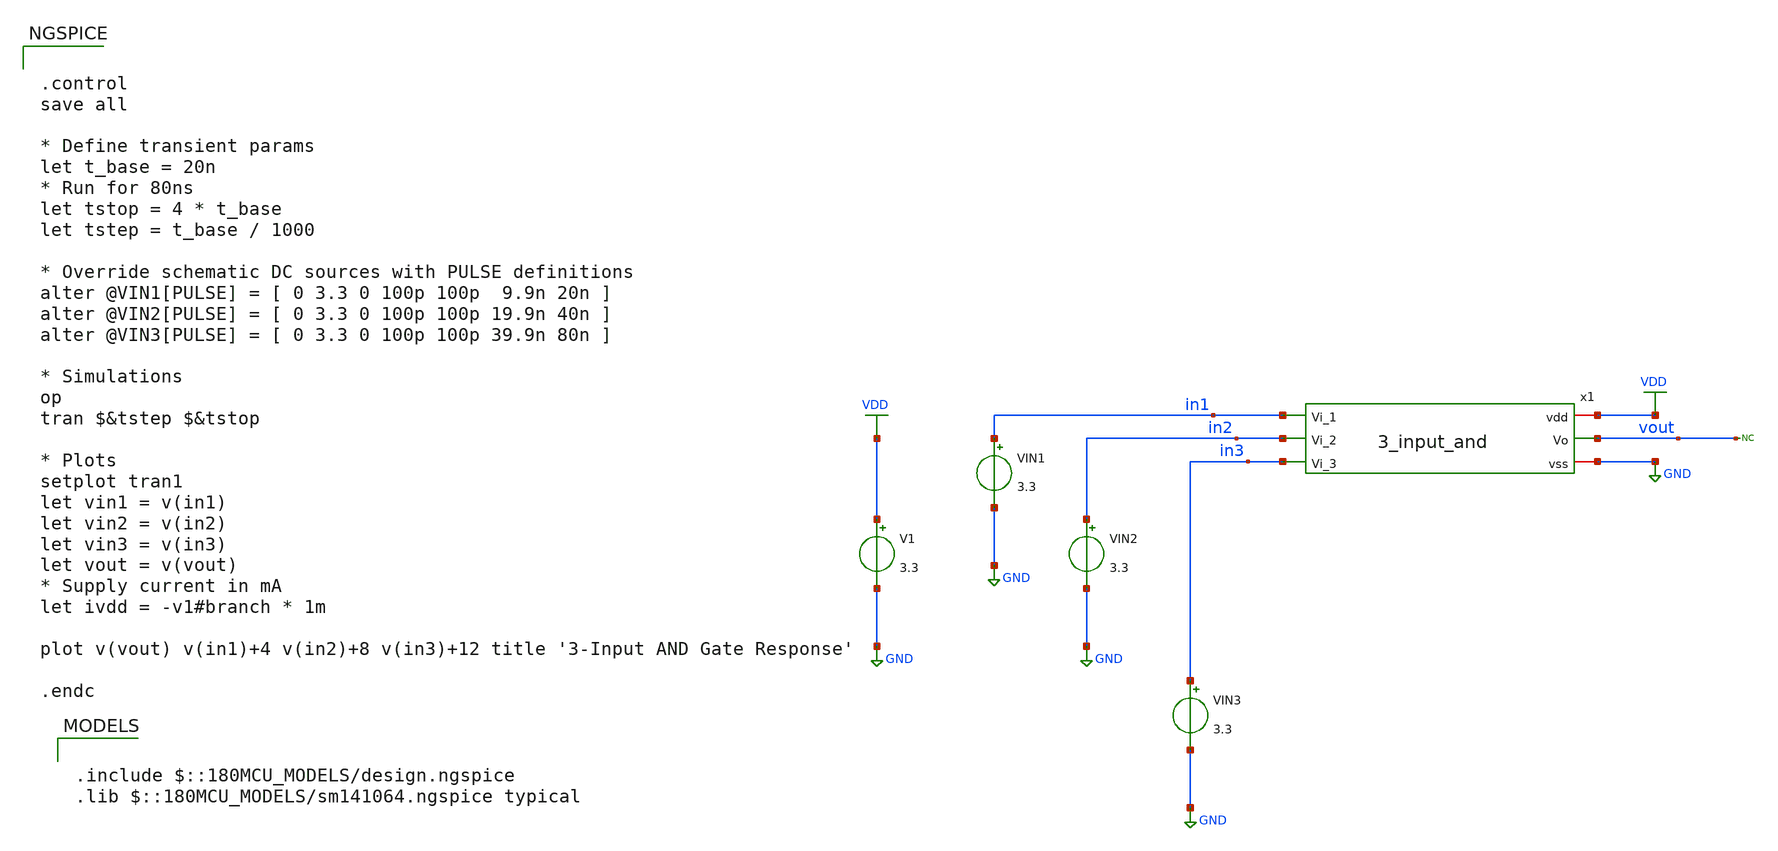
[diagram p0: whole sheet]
** sch_path: designs/3_input_and_tb.sch
**.subckt 3_input_and_tb
V1 VDD GND 3.3
VIN1 in1 GND 3.3
* noconn vout
VIN3 in3 GND 3.3
VIN2 in2 GND 3.3
x1 VDD vout in1 in2 in3 GND 3_input_and
**** begin user architecture code

.include $::180MCU_MODELS/design.ngspice
.lib $::180MCU_MODELS/sm141064.ngspice typical



.control
save all

* Define transient params
let t_base = 20n
* Run for 80ns
let tstop = 4 * t_base
let tstep = t_base / 1000

* Override schematic DC sources with PULSE definitions
alter @VIN1[PULSE] = [ 0 3.3 0 100p 100p  9.9n 20n ]
alter @VIN2[PULSE] = [ 0 3.3 0 100p 100p 19.9n 40n ]
alter @VIN3[PULSE] = [ 0 3.3 0 100p 100p 39.9n 80n ]

* Simulations
op
tran $&tstep $&tstop

* Plots
setplot tran1
let vin1 = v(in1)
let vin2 = v(in2)
let vin3 = v(in3)
let vout = v(vout)
* Supply current in mA
let ivdd = -v1#branch * 1m

plot v(vout) v(in1)+4 v(in2)+8 v(in3)+12 title '3-Input AND Gate Response'

.endc


**** end user architecture code
**.ends

* expanding   symbol:  3_input_and.sym # of pins=6
** sym_path: designs/3_input_and.sym
** sch_path: designs/3_input_and.sch
.subckt 3_input_and vdd Vo Vi_1 Vi_2 Vi_3 vss
*.iopin vdd
*.iopin vss
*.ipin Vi_1
*.ipin Vi_2
*.ipin Vi_3
*.opin Vo
XM1 net1 Vi_1 vdd vdd pfet_03v3 L=0.28u W=0.22u nf=1 ad='int((nf+1)/2) * W/nf * 0.18u' as='int((nf+2)/2) * W/nf * 0.18u'
+ pd='2*int((nf+1)/2) * (W/nf + 0.18u)' ps='2*int((nf+2)/2) * (W/nf + 0.18u)' nrd='0.18u / W' nrs='0.18u / W'
+ sa=0 sb=0 sd=0 m=1
XM2 net1 Vi_2 vdd vdd pfet_03v3 L=0.28u W=0.22u nf=1 ad='int((nf+1)/2) * W/nf * 0.18u' as='int((nf+2)/2) * W/nf * 0.18u'
+ pd='2*int((nf+1)/2) * (W/nf + 0.18u)' ps='2*int((nf+2)/2) * (W/nf + 0.18u)' nrd='0.18u / W' nrs='0.18u / W'
+ sa=0 sb=0 sd=0 m=1
XM3 net1 Vi_3 vdd vdd pfet_03v3 L=0.28u W=0.22u nf=1 ad='int((nf+1)/2) * W/nf * 0.18u' as='int((nf+2)/2) * W/nf * 0.18u'
+ pd='2*int((nf+1)/2) * (W/nf + 0.18u)' ps='2*int((nf+2)/2) * (W/nf + 0.18u)' nrd='0.18u / W' nrs='0.18u / W'
+ sa=0 sb=0 sd=0 m=1
XM4 net1 Vi_1 net3 vss nfet_03v3 L=0.28u W=0.22u nf=1 ad='int((nf+1)/2) * W/nf * 0.18u' as='int((nf+2)/2) * W/nf * 0.18u'
+ pd='2*int((nf+1)/2) * (W/nf + 0.18u)' ps='2*int((nf+2)/2) * (W/nf + 0.18u)' nrd='0.18u / W' nrs='0.18u / W'
+ sa=0 sb=0 sd=0 m=1
XM5 net3 Vi_2 net2 vss nfet_03v3 L=0.28u W=0.22u nf=1 ad='int((nf+1)/2) * W/nf * 0.18u' as='int((nf+2)/2) * W/nf * 0.18u'
+ pd='2*int((nf+1)/2) * (W/nf + 0.18u)' ps='2*int((nf+2)/2) * (W/nf + 0.18u)' nrd='0.18u / W' nrs='0.18u / W'
+ sa=0 sb=0 sd=0 m=1
XM6 net2 Vi_3 vss vss nfet_03v3 L=0.28u W=0.22u nf=1 ad='int((nf+1)/2) * W/nf * 0.18u' as='int((nf+2)/2) * W/nf * 0.18u'
+ pd='2*int((nf+1)/2) * (W/nf + 0.18u)' ps='2*int((nf+2)/2) * (W/nf + 0.18u)' nrd='0.18u / W' nrs='0.18u / W'
+ sa=0 sb=0 sd=0 m=1
XM7 Vo net1 vdd vdd pfet_03v3 L=0.28u W=0.22u nf=1 ad='int((nf+1)/2) * W/nf * 0.18u' as='int((nf+2)/2) * W/nf * 0.18u'
+ pd='2*int((nf+1)/2) * (W/nf + 0.18u)' ps='2*int((nf+2)/2) * (W/nf + 0.18u)' nrd='0.18u / W' nrs='0.18u / W'
+ sa=0 sb=0 sd=0 m=1
XM8 Vo net1 vss vss nfet_03v3 L=0.28u W=0.22u nf=1 ad='int((nf+1)/2) * W/nf * 0.18u' as='int((nf+2)/2) * W/nf * 0.18u'
+ pd='2*int((nf+1)/2) * (W/nf + 0.18u)' ps='2*int((nf+2)/2) * (W/nf + 0.18u)' nrd='0.18u / W' nrs='0.18u / W'
+ sa=0 sb=0 sd=0 m=1
.ends

.GLOBAL VDD
.GLOBAL GND
.end
